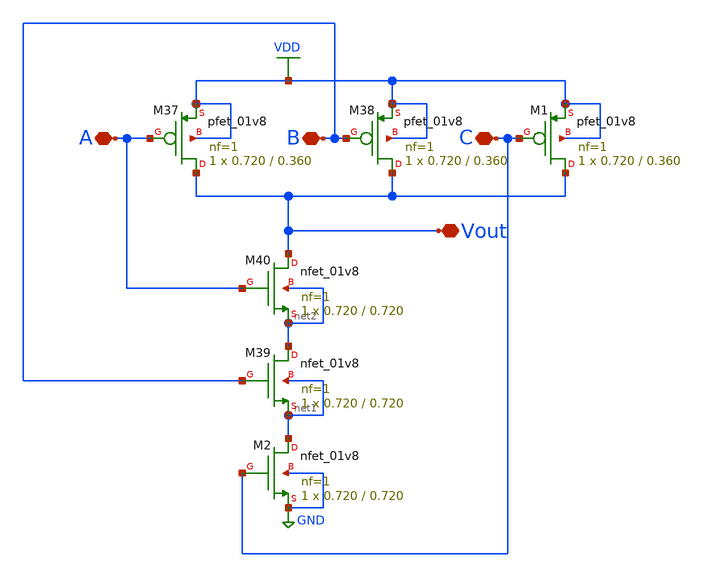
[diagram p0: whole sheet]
** sch_path: xschem/3-input-nand.sch
**.subckt 3-input-nand A B Vout C
*.iopin A
*.iopin B
*.iopin Vout
*.iopin C
XM37 Vout A VDD VDD sky130_fd_pr__pfet_01v8 L=0.360 W=0.720 nf=1 ad='int((nf+1)/2) * W/nf * 0.29' as='int((nf+2)/2) * W/nf * 0.29'
+ pd='2*int((nf+1)/2) * (W/nf + 0.29)' ps='2*int((nf+2)/2) * (W/nf + 0.29)' nrd='0.29 / W' nrs='0.29 / W'
+ sa=0 sb=0 sd=0 mult=1 m=1
XM38 Vout B VDD VDD sky130_fd_pr__pfet_01v8 L=0.360 W=0.720 nf=1 ad='int((nf+1)/2) * W/nf * 0.29' as='int((nf+2)/2) * W/nf * 0.29'
+ pd='2*int((nf+1)/2) * (W/nf + 0.29)' ps='2*int((nf+2)/2) * (W/nf + 0.29)' nrd='0.29 / W' nrs='0.29 / W'
+ sa=0 sb=0 sd=0 mult=1 m=1
XM39 net2 B net1 net1 sky130_fd_pr__nfet_01v8 L=0.720 W=0.720 nf=1 ad='int((nf+1)/2) * W/nf * 0.29' as='int((nf+2)/2) * W/nf * 0.29'
+ pd='2*int((nf+1)/2) * (W/nf + 0.29)' ps='2*int((nf+2)/2) * (W/nf + 0.29)' nrd='0.29 / W' nrs='0.29 / W'
+ sa=0 sb=0 sd=0 mult=1 m=1
XM40 Vout A net2 net2 sky130_fd_pr__nfet_01v8 L=0.720 W=0.720 nf=1 ad='int((nf+1)/2) * W/nf * 0.29' as='int((nf+2)/2) * W/nf * 0.29'
+ pd='2*int((nf+1)/2) * (W/nf + 0.29)' ps='2*int((nf+2)/2) * (W/nf + 0.29)' nrd='0.29 / W' nrs='0.29 / W'
+ sa=0 sb=0 sd=0 mult=1 m=1
XM1 Vout C VDD VDD sky130_fd_pr__pfet_01v8 L=0.360 W=0.720 nf=1 ad='int((nf+1)/2) * W/nf * 0.29' as='int((nf+2)/2) * W/nf * 0.29'
+ pd='2*int((nf+1)/2) * (W/nf + 0.29)' ps='2*int((nf+2)/2) * (W/nf + 0.29)' nrd='0.29 / W' nrs='0.29 / W'
+ sa=0 sb=0 sd=0 mult=1 m=1
XM2 net1 C GND GND sky130_fd_pr__nfet_01v8 L=0.720 W=0.720 nf=1 ad='int((nf+1)/2) * W/nf * 0.29' as='int((nf+2)/2) * W/nf * 0.29'
+ pd='2*int((nf+1)/2) * (W/nf + 0.29)' ps='2*int((nf+2)/2) * (W/nf + 0.29)' nrd='0.29 / W' nrs='0.29 / W'
+ sa=0 sb=0 sd=0 mult=1 m=1
**.ends
.GLOBAL VDD
.GLOBAL GND
.end
